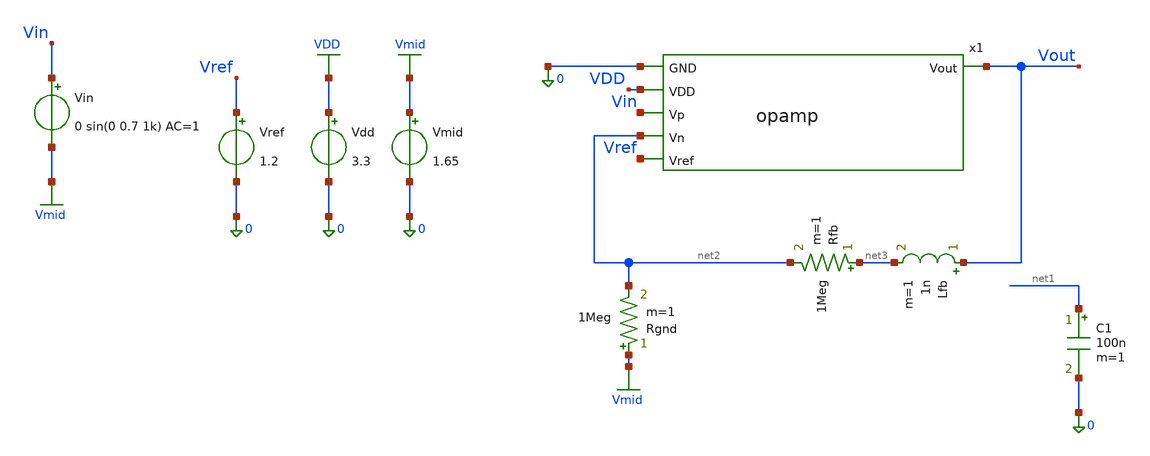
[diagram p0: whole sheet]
** sch_path: xschem/opamp_tb.sch
* Copyright 2021 Stefan Frederik Schippers
* Licensed under the Apache License, Version 2.0 (the "License");
* you may not use this file except in compliance with the License.
* You may obtain a copy of the License at
* https://www.apache.org/licenses/LICENSE-2.0
* Unless required by applicable law or agreed to in writing, software
* distributed under the License is distributed on an "AS IS" BASIS,
* WITHOUT WARRANTIES OR CONDITIONS OF ANY KIND, either express or implied.
* See the License for the specific language governing permissions and
* limitations under the License.
**.subckt opamp_tb
Vdd VDD 0 3.3
C1 net1 0 100n m=1
Vin Vin Vmid 0 sin(0 0.7 1k) AC=1
Rfb net3 net2 1Meg m=1
Rgnd Vmid net2 1Meg m=1
Vmid Vmid 0 1.65
Lfb Vout net3 1n m=1
x1 Vref Vout Vin net2 VDD 0 opamp
Vref Vref 0 1.2
**** begin user architecture code

** opencircuitdesign pdks install
.lib $::SKYWATER_MODELS/sky130.lib.spice tt



.option wnflag=1
.option savecurrents
.option rshunt=1e12
.include ../netlist/rcx/opamp.spice
.save all
.control
set gnuplot_terminal=png/quit
set units = d
op
write opamp_tb.raw
print Vref I(v.x1.x2.vmeas_iref) V(x1.x2.Vg1)
if 0
alter L5 1n
tran 1u 2m
plot V(Vin) V(Vout) title 'Vin and Vout vs time'
endif

alter Lfb 10G
ac dec 100 1 100Meg
plot db(V(Vout)) title 'Vout Open loop'
*plot cph(V(vout))*180/pi title 'Phase Vout open loop'
gnuplot opamp_ac_mag db(V(Vout))  title 'Open loop gain'  xlabel 'Freq' ylabel 'Gain dB'
gnuplot opamp_ac_phase ph(V(Vout))  title 'Open loop phase'  xlabel 'Freq' ylabel 'Phase (deg)'


if 0
alter Lfb 1n
alter Rfb 1m
ac dec 100 1 100Meg
gnuplot opamp_unity_gain db(V(Vout))  title 'Unity gain bandwidth'  xlabel 'Freq' ylabel 'Gain dB'
gnuplot opamp_unity_gain_phase cph(V(Vout))  title 'Unity gain phase'  xlabel 'Freq' ylabel 'Phase (deg)'

plot db(V(Vout)) title 'Mag Unity gain'
*plot cph(V(vout))*180/pi title 'Phase Vout Unity gain'
endif

.endc


**** end user architecture code
**.ends

* expanding   symbol:  opamp.sym # of pins=6
** sym_path: xschem/opamp.sym
** sch_path: xschem/opamp.sch
.subckt opamp Vref Vout Vp Vn VDD GND
*.opin Vout
*.ipin Vref
*.ipin Vp
*.ipin Vn
*.ipin GND
*.ipin VDD
XM1 Vg1 Vg1 net1 GND sky130_fd_pr__nfet_g5v0d10v5 L=2 W=3.33 nf=1 ad='int((1 + 1)/2) * 3.33 / 1 * 0.29'
+ as='int((1 + 2)/2) * 3.33 / 1 * 0.29' pd='2*int((1 + 1)/2) * (3.33 / 1 + 0.29)' ps='2*int((1 + 2)/2) * (3.33 / 1 + 0.29)'
+ nrd='0.29 / 3.33 ' nrs='0.29 / 3.33 ' sa=0 sb=0 sd=0 mult=3 m=3
XM2 net1 Vg1 GND GND sky130_fd_pr__nfet_g5v0d10v5 L=5 W=5 nf=1 ad='int((1 + 1)/2) * 5 / 1 * 0.29' as='int((1 + 2)/2) * 5 / 1 * 0.29'
+ pd='2*int((1 + 1)/2) * (5 / 1 + 0.29)' ps='2*int((1 + 2)/2) * (5 / 1 + 0.29)' nrd='0.29 / 5 ' nrs='0.29 / 5 '
+ sa=0 sb=0 sd=0 mult=1 m=1
XM4 net2 Vg1 GND GND sky130_fd_pr__nfet_g5v0d10v5 L=5 W=5 nf=1 ad='int((1 + 1)/2) * 5 / 1 * 0.29' as='int((1 + 2)/2) * 5 / 1 * 0.29'
+ pd='2*int((1 + 1)/2) * (5 / 1 + 0.29)' ps='2*int((1 + 2)/2) * (5 / 1 + 0.29)' nrd='0.29 / 5 ' nrs='0.29 / 5 '
+ sa=0 sb=0 sd=0 mult=1 m=1
XM3 Vg5 Vg1 net2 GND sky130_fd_pr__nfet_g5v0d10v5 L=2 W=3.33 nf=1 ad='int((1 + 1)/2) * 3.33 / 1 * 0.29'
+ as='int((1 + 2)/2) * 3.33 / 1 * 0.29' pd='2*int((1 + 1)/2) * (3.33 / 1 + 0.29)' ps='2*int((1 + 2)/2) * (3.33 / 1 + 0.29)'
+ nrd='0.29 / 3.33 ' nrs='0.29 / 3.33 ' sa=0 sb=0 sd=0 mult=3 m=3
XMr1 net6 Vref GND GND sky130_fd_pr__nfet_g5v0d10v5 L=8 W=5 nf=1 ad='int((1 + 1)/2) * 5 / 1 * 0.29' as='int((1 + 2)/2) * 5 / 1 * 0.29'
+ pd='2*int((1 + 1)/2) * (5 / 1 + 0.29)' ps='2*int((1 + 2)/2) * (5 / 1 + 0.29)' nrd='0.29 / 5 ' nrs='0.29 / 5 '
+ sa=0 sb=0 sd=0 mult=1 m=1
XMr2 VgR2 VgR2 VDD VDD sky130_fd_pr__pfet_g5v0d10v5 L=5 W=4 nf=1 ad='int((1 + 1)/2) * 4 / 1 * 0.29' as='int((1 + 2)/2) * 4 / 1 * 0.29'
+ pd='2*int((1 + 1)/2) * (4 / 1 + 0.29)' ps='2*int((1 + 2)/2) * (4 / 1 + 0.29)' nrd='0.29 / 4 ' nrs='0.29 / 4 '
+ sa=0 sb=0 sd=0 mult=1 m=1
XMr3 Vg1 VgR2 VDD VDD sky130_fd_pr__pfet_g5v0d10v5 L=5 W=4 nf=1 ad='int((1 + 1)/2) * 4 / 1 * 0.29' as='int((1 + 2)/2) * 4 / 1 * 0.29'
+ pd='2*int((1 + 1)/2) * (4 / 1 + 0.29)' ps='2*int((1 + 2)/2) * (4 / 1 + 0.29)' nrd='0.29 / 4 ' nrs='0.29 / 4 '
+ sa=0 sb=0 sd=0 mult=1 m=1
XM32 net3 Vg1 GND GND sky130_fd_pr__nfet_g5v0d10v5 L=5 W=10 nf=1 ad='int((1 + 1)/2) * 10 / 1 * 0.29'
+ as='int((1 + 2)/2) * 10 / 1 * 0.29' pd='2*int((1 + 1)/2) * (10 / 1 + 0.29)' ps='2*int((1 + 2)/2) * (10 / 1 + 0.29)'
+ nrd='0.29 / 10 ' nrs='0.29 / 10 ' sa=0 sb=0 sd=0 mult=1 m=1
XM31 Vs29 Vg1 net3 GND sky130_fd_pr__nfet_g5v0d10v5 L=2 W=6.66 nf=1 ad='int((1 + 1)/2) * 6.66 / 1 * 0.29'
+ as='int((1 + 2)/2) * 6.66 / 1 * 0.29' pd='2*int((1 + 1)/2) * (6.66 / 1 + 0.29)' ps='2*int((1 + 2)/2) * (6.66 / 1 + 0.29)'
+ nrd='0.29 / 6.66 ' nrs='0.29 / 6.66 ' sa=0 sb=0 sd=0 mult=3 m=3
XM15 Vg11 Vg1 Vd10 GND sky130_fd_pr__nfet_g5v0d10v5 L=2 W=14.3 nf=1 ad='int((1 + 1)/2) * 14.3 / 1 * 0.29'
+ as='int((1 + 2)/2) * 14.3 / 1 * 0.29' pd='2*int((1 + 1)/2) * (14.3 / 1 + 0.29)' ps='2*int((1 + 2)/2) * (14.3 / 1 + 0.29)'
+ nrd='0.29 / 14.3 ' nrs='0.29 / 14.3 ' sa=0 sb=0 sd=0 mult=7 m=7
XM16 Vd10 Vg1 GND GND sky130_fd_pr__nfet_g5v0d10v5 L=5 W=10 nf=1 ad='int((1 + 1)/2) * 10 / 1 * 0.29'
+ as='int((1 + 2)/2) * 10 / 1 * 0.29' pd='2*int((1 + 1)/2) * (10 / 1 + 0.29)' ps='2*int((1 + 2)/2) * (10 / 1 + 0.29)'
+ nrd='0.29 / 10 ' nrs='0.29 / 10 ' sa=0 sb=0 sd=0 mult=1 m=1
XM18 Vd9 Vg1 GND GND sky130_fd_pr__nfet_g5v0d10v5 L=5 W=10 nf=1 ad='int((1 + 1)/2) * 10 / 1 * 0.29' as='int((1 + 2)/2) * 10 / 1 * 0.29'
+ pd='2*int((1 + 1)/2) * (10 / 1 + 0.29)' ps='2*int((1 + 2)/2) * (10 / 1 + 0.29)' nrd='0.29 / 10 ' nrs='0.29 / 10 '
+ sa=0 sb=0 sd=0 mult=1 m=1
XM17 Vg28 Vg1 Vd9 GND sky130_fd_pr__nfet_g5v0d10v5 L=2 W=14.3 nf=1 ad='int((1 + 1)/2) * 14.3 / 1 * 0.29'
+ as='int((1 + 2)/2) * 14.3 / 1 * 0.29' pd='2*int((1 + 1)/2) * (14.3 / 1 + 0.29)' ps='2*int((1 + 2)/2) * (14.3 / 1 + 0.29)'
+ nrd='0.29 / 14.3 ' nrs='0.29 / 14.3 ' sa=0 sb=0 sd=0 mult=7 m=7
XM20 Vg22 Vg1 GND GND sky130_fd_pr__nfet_g5v0d10v5 L=5 W=1.5 nf=1 ad='int((1 + 1)/2) * 1.5 / 1 * 0.29'
+ as='int((1 + 2)/2) * 1.5 / 1 * 0.29' pd='2*int((1 + 1)/2) * (1.5 / 1 + 0.29)' ps='2*int((1 + 2)/2) * (1.5 / 1 + 0.29)'
+ nrd='0.29 / 1.5 ' nrs='0.29 / 1.5 ' sa=0 sb=0 sd=0 mult=1 m=1
XM26 Vg26 Vg26 GND GND sky130_fd_pr__nfet_g5v0d10v5 L=0.5 W=5 nf=1 ad='int((1 + 1)/2) * 5 / 1 * 0.29'
+ as='int((1 + 2)/2) * 5 / 1 * 0.29' pd='2*int((1 + 1)/2) * (5 / 1 + 0.29)' ps='2*int((1 + 2)/2) * (5 / 1 + 0.29)'
+ nrd='0.29 / 5 ' nrs='0.29 / 5 ' sa=0 sb=0 sd=0 mult=5 m=5
XM25 Vd24 Vd24 Vg26 GND sky130_fd_pr__nfet_g5v0d10v5 L=0.5 W=5 nf=1 ad='int((1 + 1)/2) * 5 / 1 * 0.29'
+ as='int((1 + 2)/2) * 5 / 1 * 0.29' pd='2*int((1 + 1)/2) * (5 / 1 + 0.29)' ps='2*int((1 + 2)/2) * (5 / 1 + 0.29)'
+ nrd='0.29 / 5 ' nrs='0.29 / 5 ' sa=0 sb=0 sd=0 mult=5 m=5
XM23 Vg27 Vd24 Vg28 GND sky130_fd_pr__nfet_g5v0d10v5 L=0.5 W=10 nf=1 ad='int((1 + 1)/2) * 10 / 1 * 0.29'
+ as='int((1 + 2)/2) * 10 / 1 * 0.29' pd='2*int((1 + 1)/2) * (10 / 1 + 0.29)' ps='2*int((1 + 2)/2) * (10 / 1 + 0.29)'
+ nrd='0.29 / 10 ' nrs='0.29 / 10 ' sa=0 sb=0 sd=0 mult=5 m=5
XM28 Vout Vg28 GND GND sky130_fd_pr__nfet_g5v0d10v5 L=0.5 W=10 nf=1 ad='int((1 + 1)/2) * 10 / 1 * 0.29'
+ as='int((1 + 2)/2) * 10 / 1 * 0.29' pd='2*int((1 + 1)/2) * (10 / 1 + 0.29)' ps='2*int((1 + 2)/2) * (10 / 1 + 0.29)'
+ nrd='0.29 / 10 ' nrs='0.29 / 10 ' sa=0 sb=0 sd=0 mult=15 m=15
XM30 Vd30 Vn Vs29 GND sky130_fd_pr__nfet_g5v0d10v5 L=1.5 W=11.11 nf=1 ad='int((1 + 1)/2) * 11.11 / 1 * 0.29'
+ as='int((1 + 2)/2) * 11.11 / 1 * 0.29' pd='2*int((1 + 1)/2) * (11.11 / 1 + 0.29)' ps='2*int((1 + 2)/2) * (11.11 / 1 + 0.29)'
+ nrd='0.29 / 11.11 ' nrs='0.29 / 11.11 ' sa=0 sb=0 sd=0 mult=9 m=9
XM29 Vd29 Vp Vs29 GND sky130_fd_pr__nfet_g5v0d10v5 L=1.5 W=11.11 nf=1 ad='int((1 + 1)/2) * 11.11 / 1 * 0.29'
+ as='int((1 + 2)/2) * 11.11 / 1 * 0.29' pd='2*int((1 + 1)/2) * (11.11 / 1 + 0.29)' ps='2*int((1 + 2)/2) * (11.11 / 1 + 0.29)'
+ nrd='0.29 / 11.11 ' nrs='0.29 / 11.11 ' sa=0 sb=0 sd=0 mult=9 m=9
XM5 net4 Vg5 VDD VDD sky130_fd_pr__pfet_g5v0d10v5 L=5 W=5 nf=1 ad='int((1 + 1)/2) * 5 / 1 * 0.29' as='int((1 + 2)/2) * 5 / 1 * 0.29'
+ pd='2*int((1 + 1)/2) * (5 / 1 + 0.29)' ps='2*int((1 + 2)/2) * (5 / 1 + 0.29)' nrd='0.29 / 5 ' nrs='0.29 / 5 '
+ sa=0 sb=0 sd=0 mult=3 m=3
XM6 Vg5 Vg5 net4 VDD sky130_fd_pr__pfet_g5v0d10v5 L=2 W=6.6 nf=1 ad='int((1 + 1)/2) * 6.6 / 1 * 0.29'
+ as='int((1 + 2)/2) * 6.6 / 1 * 0.29' pd='2*int((1 + 1)/2) * (6.6 / 1 + 0.29)' ps='2*int((1 + 2)/2) * (6.6 / 1 + 0.29)'
+ nrd='0.29 / 6.6 ' nrs='0.29 / 6.6 ' sa=0 sb=0 sd=0 mult=3 m=3
XM7 net5 Vg5 VDD VDD sky130_fd_pr__pfet_g5v0d10v5 L=5 W=10 nf=1 ad='int((1 + 1)/2) * 10 / 1 * 0.29' as='int((1 + 2)/2) * 10 / 1 * 0.29'
+ pd='2*int((1 + 1)/2) * (10 / 1 + 0.29)' ps='2*int((1 + 2)/2) * (10 / 1 + 0.29)' nrd='0.29 / 10 ' nrs='0.29 / 10 '
+ sa=0 sb=0 sd=0 mult=3 m=3
XM8 Vd8 Vg5 net5 VDD sky130_fd_pr__pfet_g5v0d10v5 L=2 W=13.2 nf=1 ad='int((1 + 1)/2) * 13.2 / 1 * 0.29'
+ as='int((1 + 2)/2) * 13.2 / 1 * 0.29' pd='2*int((1 + 1)/2) * (13.2 / 1 + 0.29)' ps='2*int((1 + 2)/2) * (13.2 / 1 + 0.29)'
+ nrd='0.29 / 13.2 ' nrs='0.29 / 13.2 ' sa=0 sb=0 sd=0 mult=3 m=3
XM09 Vd9 Vp Vd8 Vd8 sky130_fd_pr__pfet_g5v0d10v5 L=1.5 W=22.22 nf=1 ad='int((1 + 1)/2) * 22.22 / 1 * 0.29'
+ as='int((1 + 2)/2) * 22.22 / 1 * 0.29' pd='2*int((1 + 1)/2) * (22.22 / 1 + 0.29)' ps='2*int((1 + 2)/2) * (22.22 / 1 + 0.29)'
+ nrd='0.29 / 22.22 ' nrs='0.29 / 22.22 ' sa=0 sb=0 sd=0 mult=9 m=9
XM010 Vd10 Vn Vd8 Vd8 sky130_fd_pr__pfet_g5v0d10v5 L=1.5 W=22.22 nf=1 ad='int((1 + 1)/2) * 22.22 / 1 * 0.29'
+ as='int((1 + 2)/2) * 22.22 / 1 * 0.29' pd='2*int((1 + 1)/2) * (22.22 / 1 + 0.29)' ps='2*int((1 + 2)/2) * (22.22 / 1 + 0.29)'
+ nrd='0.29 / 22.22 ' nrs='0.29 / 22.22 ' sa=0 sb=0 sd=0 mult=9 m=9
XM13 Vd29 Vg11 VDD VDD sky130_fd_pr__pfet_g5v0d10v5 L=2.5 W=10 nf=1 ad='int((1 + 1)/2) * 10 / 1 * 0.29'
+ as='int((1 + 2)/2) * 10 / 1 * 0.29' pd='2*int((1 + 1)/2) * (10 / 1 + 0.29)' ps='2*int((1 + 2)/2) * (10 / 1 + 0.29)'
+ nrd='0.29 / 10 ' nrs='0.29 / 10 ' sa=0 sb=0 sd=0 mult=5 m=5
XM14 Vg27 Vg11 Vd29 VDD sky130_fd_pr__pfet_g5v0d10v5 L=1 W=10 nf=1 ad='int((1 + 1)/2) * 10 / 1 * 0.29'
+ as='int((1 + 2)/2) * 10 / 1 * 0.29' pd='2*int((1 + 1)/2) * (10 / 1 + 0.29)' ps='2*int((1 + 2)/2) * (10 / 1 + 0.29)'
+ nrd='0.29 / 10 ' nrs='0.29 / 10 ' sa=0 sb=0 sd=0 mult=5 m=5
XM11 Vd30 Vg11 VDD VDD sky130_fd_pr__pfet_g5v0d10v5 L=2.5 W=10 nf=1 ad='int((1 + 1)/2) * 10 / 1 * 0.29'
+ as='int((1 + 2)/2) * 10 / 1 * 0.29' pd='2*int((1 + 1)/2) * (10 / 1 + 0.29)' ps='2*int((1 + 2)/2) * (10 / 1 + 0.29)'
+ nrd='0.29 / 10 ' nrs='0.29 / 10 ' sa=0 sb=0 sd=0 mult=5 m=5
XM12 Vg11 Vg11 Vd30 VDD sky130_fd_pr__pfet_g5v0d10v5 L=1 W=10 nf=1 ad='int((1 + 1)/2) * 10 / 1 * 0.29'
+ as='int((1 + 2)/2) * 10 / 1 * 0.29' pd='2*int((1 + 1)/2) * (10 / 1 + 0.29)' ps='2*int((1 + 2)/2) * (10 / 1 + 0.29)'
+ nrd='0.29 / 10 ' nrs='0.29 / 10 ' sa=0 sb=0 sd=0 mult=5 m=5
XM021 Vg21 Vg21 VDD VDD sky130_fd_pr__pfet_g5v0d10v5 L=0.5 W=15 nf=1 ad='int((1 + 1)/2) * 15 / 1 * 0.29'
+ as='int((1 + 2)/2) * 15 / 1 * 0.29' pd='2*int((1 + 1)/2) * (15 / 1 + 0.29)' ps='2*int((1 + 2)/2) * (15 / 1 + 0.29)'
+ nrd='0.29 / 15 ' nrs='0.29 / 15 ' sa=0 sb=0 sd=0 mult=5 m=5
XM022 Vg22 Vg22 Vg21 VDD sky130_fd_pr__pfet_g5v0d10v5 L=0.5 W=15 nf=1 ad='int((1 + 1)/2) * 15 / 1 * 0.29'
+ as='int((1 + 2)/2) * 15 / 1 * 0.29' pd='2*int((1 + 1)/2) * (15 / 1 + 0.29)' ps='2*int((1 + 2)/2) * (15 / 1 + 0.29)'
+ nrd='0.29 / 15 ' nrs='0.29 / 15 ' sa=0 sb=0 sd=0 mult=5 m=5
XM24 Vd24 Vg5 VDD VDD sky130_fd_pr__pfet_g5v0d10v5 L=5 W=4 nf=1 ad='int((1 + 1)/2) * 4 / 1 * 0.29' as='int((1 + 2)/2) * 4 / 1 * 0.29'
+ pd='2*int((1 + 1)/2) * (4 / 1 + 0.29)' ps='2*int((1 + 2)/2) * (4 / 1 + 0.29)' nrd='0.29 / 4 ' nrs='0.29 / 4 '
+ sa=0 sb=0 sd=0 mult=1 m=1
XM27 Vout Vg27 VDD VDD sky130_fd_pr__pfet_g5v0d10v5 L=0.5 W=15 nf=1 ad='int((1 + 1)/2) * 15 / 1 * 0.29'
+ as='int((1 + 2)/2) * 15 / 1 * 0.29' pd='2*int((1 + 1)/2) * (15 / 1 + 0.29)' ps='2*int((1 + 2)/2) * (15 / 1 + 0.29)'
+ nrd='0.29 / 15 ' nrs='0.29 / 15 ' sa=0 sb=0 sd=0 mult=25 m=25
XM19 Vg28 Vg22 Vg27 VDD sky130_fd_pr__pfet_g5v0d10v5 L=0.5 W=10 nf=1 ad='int((1 + 1)/2) * 10 / 1 * 0.29'
+ as='int((1 + 2)/2) * 10 / 1 * 0.29' pd='2*int((1 + 1)/2) * (10 / 1 + 0.29)' ps='2*int((1 + 2)/2) * (10 / 1 + 0.29)'
+ nrd='0.29 / 10 ' nrs='0.29 / 10 ' sa=0 sb=0 sd=0 mult=15 m=15
Vmeas_Iref VgR2 net6 0
.save i(vmeas_iref)
XC1 Vg27 Vout sky130_fd_pr__cap_mim_m3_1 W=30 L=20 MF=4 m=4
XC2 Vg28 Vout sky130_fd_pr__cap_mim_m3_1 W=30 L=20 MF=4 m=4
.ends

.GLOBAL VDD
.GLOBAL Vmid
.GLOBAL GND
.end
